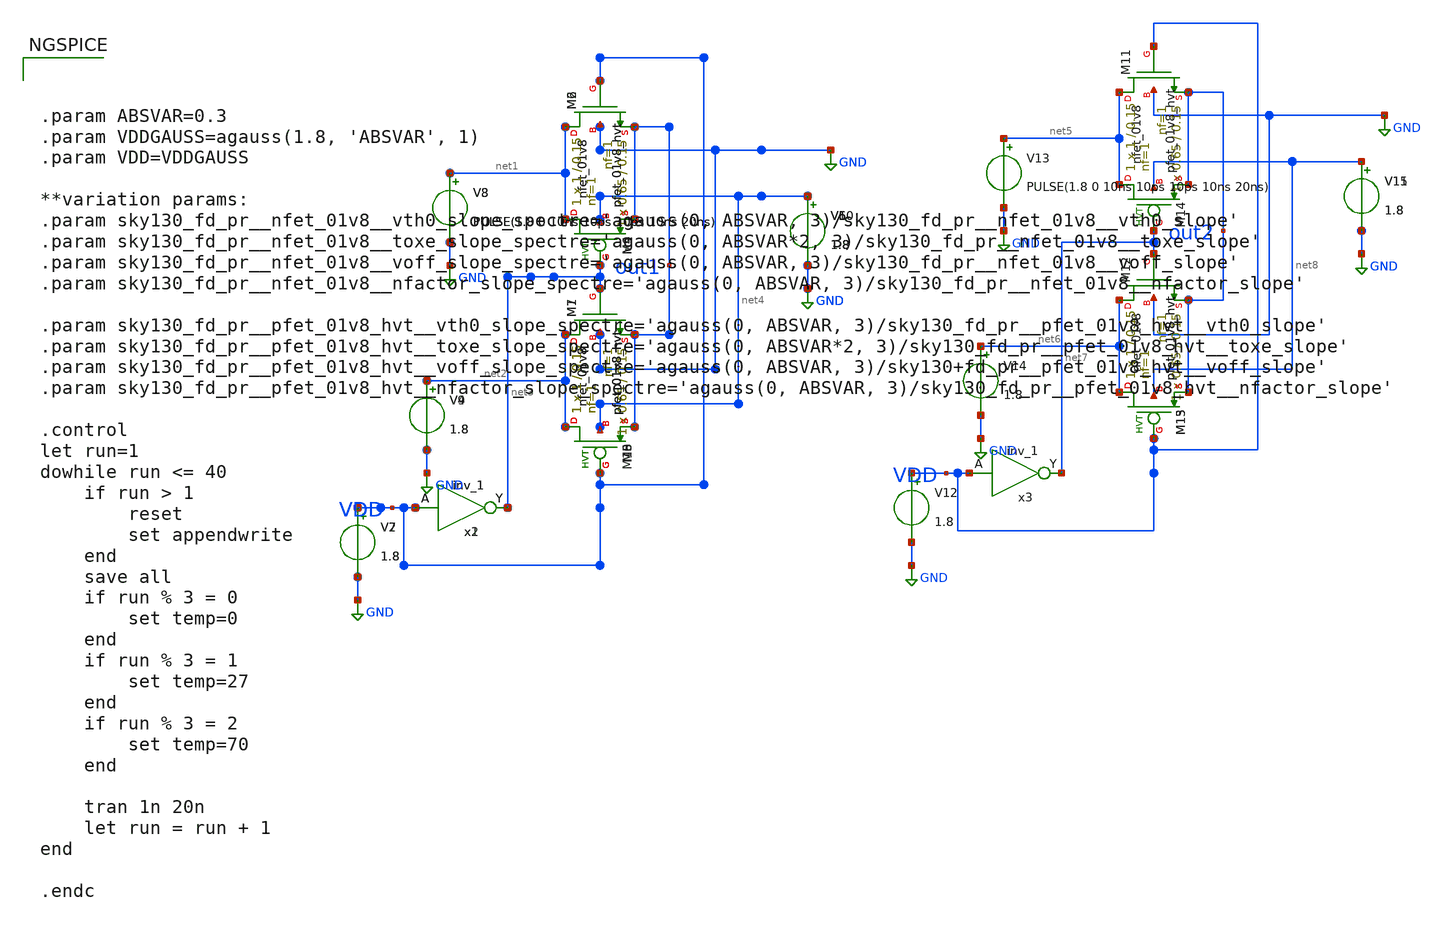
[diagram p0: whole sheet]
** sch_path: xiaolin/mc_test.sch
**.subckt mc_test
XM2 net1 VDD out1 GND sky130_fd_pr__nfet_01v8 L=0.15 W=0.65 nf=1 ad='int((nf+1)/2) * W/nf * 0.29' as='int((nf+2)/2) * W/nf * 0.29'
+ pd='2*int((nf+1)/2) * (W/nf + 0.29)' ps='2*int((nf+2)/2) * (W/nf + 0.29)' nrd='0.29 / W' nrs='0.29 / W'
+ sa=0 sb=0 sd=0 mult=1 m=1
XM1 net2 net3 out1 GND sky130_fd_pr__nfet_01v8 L=0.15 W=0.65 nf=1 ad='int((nf+1)/2) * W/nf * 0.29' as='int((nf+2)/2) * W/nf * 0.29'
+ pd='2*int((nf+1)/2) * (W/nf + 0.29)' ps='2*int((nf+2)/2) * (W/nf + 0.29)' nrd='0.29 / W' nrs='0.29 / W'
+ sa=0 sb=0 sd=0 mult=1 m=1
XM3 net2 VDD out1 net4 sky130_fd_pr__pfet_01v8_hvt L=0.15 W=1 nf=1 ad='int((nf+1)/2) * W/nf * 0.29' as='int((nf+2)/2) * W/nf * 0.29'
+ pd='2*int((nf+1)/2) * (W/nf + 0.29)' ps='2*int((nf+2)/2) * (W/nf + 0.29)' nrd='0.29 / W' nrs='0.29 / W'
+ sa=0 sb=0 sd=0 mult=1 m=1
XM4 net1 net3 out1 net4 sky130_fd_pr__pfet_01v8_hvt L=0.15 W=1 nf=1 ad='int((nf+1)/2) * W/nf * 0.29'
+ as='int((nf+2)/2) * W/nf * 0.29' pd='2*int((nf+1)/2) * (W/nf + 0.29)' ps='2*int((nf+2)/2) * (W/nf + 0.29)'
+ nrd='0.29 / W' nrs='0.29 / W' sa=0 sb=0 sd=0 mult=1 m=1
XM5 net2 VDD out1 net4 sky130_fd_pr__pfet_01v8_hvt L=0.15 W=1 nf=1 ad='int((nf+1)/2) * W/nf * 0.29' as='int((nf+2)/2) * W/nf * 0.29'
+ pd='2*int((nf+1)/2) * (W/nf + 0.29)' ps='2*int((nf+2)/2) * (W/nf + 0.29)' nrd='0.29 / W' nrs='0.29 / W'
+ sa=0 sb=0 sd=0 mult=1 m=1
V1 net4 GND 1.8
x1 VDD GND GND VDD VDD net3 sky130_fd_sc_hd__inv_1
V2 VDD GND 1.8
V3 net1 GND PULSE(1.8 0 10ns 10ps 10ps 10ns 20ns)
V4 net2 GND 1.8
V5 net4 GND 1.8
XM6 net1 VDD out1 GND sky130_fd_pr__nfet_01v8 L=0.15 W=0.65 nf=1 ad='int((nf+1)/2) * W/nf * 0.29' as='int((nf+2)/2) * W/nf * 0.29'
+ pd='2*int((nf+1)/2) * (W/nf + 0.29)' ps='2*int((nf+2)/2) * (W/nf + 0.29)' nrd='0.29 / W' nrs='0.29 / W'
+ sa=0 sb=0 sd=0 mult=1 m=1
XM7 net2 net3 out1 GND sky130_fd_pr__nfet_01v8 L=0.15 W=0.65 nf=1 ad='int((nf+1)/2) * W/nf * 0.29' as='int((nf+2)/2) * W/nf * 0.29'
+ pd='2*int((nf+1)/2) * (W/nf + 0.29)' ps='2*int((nf+2)/2) * (W/nf + 0.29)' nrd='0.29 / W' nrs='0.29 / W'
+ sa=0 sb=0 sd=0 mult=1 m=1
XM8 net2 VDD out1 net4 sky130_fd_pr__pfet_01v8_hvt L=0.15 W=1 nf=1 ad='int((nf+1)/2) * W/nf * 0.29' as='int((nf+2)/2) * W/nf * 0.29'
+ pd='2*int((nf+1)/2) * (W/nf + 0.29)' ps='2*int((nf+2)/2) * (W/nf + 0.29)' nrd='0.29 / W' nrs='0.29 / W'
+ sa=0 sb=0 sd=0 mult=1 m=1
XM9 net1 net3 out1 net4 sky130_fd_pr__pfet_01v8_hvt L=0.15 W=1 nf=1 ad='int((nf+1)/2) * W/nf * 0.29'
+ as='int((nf+2)/2) * W/nf * 0.29' pd='2*int((nf+1)/2) * (W/nf + 0.29)' ps='2*int((nf+2)/2) * (W/nf + 0.29)'
+ nrd='0.29 / W' nrs='0.29 / W' sa=0 sb=0 sd=0 mult=1 m=1
XM10 net2 VDD out1 net4 sky130_fd_pr__pfet_01v8_hvt L=0.15 W=1 nf=1 ad='int((nf+1)/2) * W/nf * 0.29'
+ as='int((nf+2)/2) * W/nf * 0.29' pd='2*int((nf+1)/2) * (W/nf + 0.29)' ps='2*int((nf+2)/2) * (W/nf + 0.29)'
+ nrd='0.29 / W' nrs='0.29 / W' sa=0 sb=0 sd=0 mult=1 m=1
V6 net4 GND 1.8
x2 VDD GND GND VDD VDD net3 sky130_fd_sc_hd__inv_1
V7 VDD GND 1.8
V8 net1 GND PULSE(1.8 0 10ns 10ps 10ps 10ns 20ns)
V9 net2 GND 1.8
V10 net4 GND 1.8
XM11 net5 VDD out2 GND sky130_fd_pr__nfet_01v8 L=0.15 W=0.65 nf=1 ad='int((nf+1)/2) * W/nf * 0.29' as='int((nf+2)/2) * W/nf * 0.29'
+ pd='2*int((nf+1)/2) * (W/nf + 0.29)' ps='2*int((nf+2)/2) * (W/nf + 0.29)' nrd='0.29 / W' nrs='0.29 / W'
+ sa=0 sb=0 sd=0 mult=1 m=1
XM12 net6 net7 out2 GND sky130_fd_pr__nfet_01v8 L=0.15 W=0.65 nf=1 ad='int((nf+1)/2) * W/nf * 0.29' as='int((nf+2)/2) * W/nf * 0.29'
+ pd='2*int((nf+1)/2) * (W/nf + 0.29)' ps='2*int((nf+2)/2) * (W/nf + 0.29)' nrd='0.29 / W' nrs='0.29 / W'
+ sa=0 sb=0 sd=0 mult=1 m=1
XM13 net6 VDD out2 net8 sky130_fd_pr__pfet_01v8_hvt L=0.15 W=1 nf=1 ad='int((nf+1)/2) * W/nf * 0.29'
+ as='int((nf+2)/2) * W/nf * 0.29' pd='2*int((nf+1)/2) * (W/nf + 0.29)' ps='2*int((nf+2)/2) * (W/nf + 0.29)'
+ nrd='0.29 / W' nrs='0.29 / W' sa=0 sb=0 sd=0 mult=1 m=1
XM14 net5 net7 out2 net8 sky130_fd_pr__pfet_01v8_hvt L=0.15 W=1 nf=1 ad='int((nf+1)/2) * W/nf * 0.29'
+ as='int((nf+2)/2) * W/nf * 0.29' pd='2*int((nf+1)/2) * (W/nf + 0.29)' ps='2*int((nf+2)/2) * (W/nf + 0.29)'
+ nrd='0.29 / W' nrs='0.29 / W' sa=0 sb=0 sd=0 mult=1 m=1
XM15 net6 VDD out2 net8 sky130_fd_pr__pfet_01v8_hvt L=0.15 W=1 nf=1 ad='int((nf+1)/2) * W/nf * 0.29'
+ as='int((nf+2)/2) * W/nf * 0.29' pd='2*int((nf+1)/2) * (W/nf + 0.29)' ps='2*int((nf+2)/2) * (W/nf + 0.29)'
+ nrd='0.29 / W' nrs='0.29 / W' sa=0 sb=0 sd=0 mult=1 m=1
V11 net8 GND 1.8
x3 VDD GND GND VDD VDD net7 sky130_fd_sc_hd__inv_1
V12 VDD GND 1.8
V13 net5 GND PULSE(1.8 0 10ns 10ps 10ps 10ns 20ns)
V14 net6 GND 1.8
V15 net8 GND 1.8
**** begin user architecture code

.lib ~/372puf/ee372/sky130A/libs.tech/ngspice/sky130.lib.spice
.include ~/372puf/ee372/sky130A/libs.ref/sky130_fd_pr/spice/sky130_fd_pr__nfet_01v8__tt.pm3.spice
.include ~/372puf/ee372/sky130A/libs.ref/sky130_fd_pr/spice/sky130_fd_pr__pfet_01v8_hvt__tt.pm3.spice

.include ~/372puf/ee372/sky130A/libs.ref/sky130_fd_sc_hd/spice/sky130_fd_sc_hd.spice

*mismatch parameters
.include ~/372puf/ee372/sky130A/libs.ref/sky130_fd_pr/spice/sky130_fd_pr__nfet_01v8__mismatch.corner.spice
.include ~/372puf/ee372/sky130A/libs.ref/sky130_fd_pr/spice/sky130_fd_pr__pfet_01v8_hvt__mismatch.corner.spice

*
.include ~/372puf/ee372/sky130A/libs.ref/sky130_fd_pr/spice/sky130_fd_pr__nfet_01v8__tt.corner.spice
.include ~/372puf/ee372/sky130A/libs.ref/sky130_fd_pr/spice/sky130_fd_pr__pfet_01v8_hvt__tt.corner.spice







.param ABSVAR=0.3
.param VDDGAUSS=agauss(1.8, 'ABSVAR', 1)
.param VDD=VDDGAUSS

**variation params:
.param sky130_fd_pr__nfet_01v8__vth0_slope_spectre='agauss(0, ABSVAR, 3)/sky130_fd_pr__nfet_01v8__vth0_slope'
.param sky130_fd_pr__nfet_01v8__toxe_slope_spectre='agauss(0, ABSVAR*2, 3)/sky130_fd_pr__nfet_01v8__toxe_slope'
.param sky130_fd_pr__nfet_01v8__voff_slope_spectre='agauss(0, ABSVAR, 3)/sky130_fd_pr__nfet_01v8__voff_slope'
.param sky130_fd_pr__nfet_01v8__nfactor_slope_spectre='agauss(0, ABSVAR, 3)/sky130_fd_pr__nfet_01v8__nfactor_slope'

.param sky130_fd_pr__pfet_01v8_hvt__vth0_slope_spectre='agauss(0, ABSVAR, 3)/sky130_fd_pr__pfet_01v8_hvt__vth0_slope'
.param sky130_fd_pr__pfet_01v8_hvt__toxe_slope_spectre='agauss(0, ABSVAR*2, 3)/sky130_fd_pr__pfet_01v8_hvt__toxe_slope'
.param sky130_fd_pr__pfet_01v8_hvt__voff_slope_spectre='agauss(0, ABSVAR, 3)/sky130+fd_pr__pfet_01v8_hvt__voff_slope'
.param sky130_fd_pr__pfet_01v8_hvt__nfactor_slope_spectre='agauss(0, ABSVAR, 3)/sky130_fd_pr__pfet_01v8_hvt__nfactor_slope'

.control
let run=1
dowhile run <= 40
	if run > 1
		reset
		set appendwrite
	end
	save all
	if run % 3 = 0
		set temp=0
	end
	if run % 3 = 1
		set temp=27
	end
	if run % 3 = 2
		set temp=70
	end

	tran 1n 20n
	let run = run + 1
end

.endc


**** end user architecture code
**.ends
.GLOBAL GND
.end
